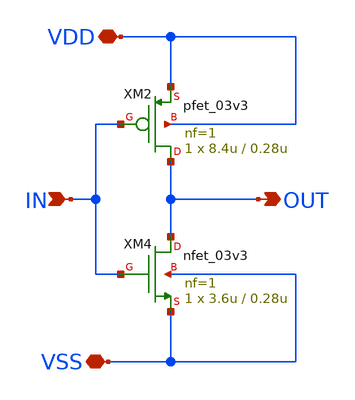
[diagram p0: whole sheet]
** sch_path: xschem/io_inv_3i.sch
* Copyright 2023 David Mitchell Bailey
* Licensed under the Apache License, Version 2.0 (the "License");
* you may not use this file except in compliance with the License.
* You may obtain a copy of the License at
* https://www.apache.org/licenses/LICENSE-2.0
* Unless required by applicable law or agreed to in writing, software
* distributed under the License is distributed on an "AS IS" BASIS,
* WITHOUT WARRANTIES OR CONDITIONS OF ANY KIND, either express or implied.
* See the License for the specific language governing permissions and
* limitations under the License.
**.subckt io_inv_3i OUT IN VDD VSS
*.opin OUT
*.ipin IN
*.iopin VDD
*.iopin VSS
XM2 OUT IN VDD VDD pfet_03v3 L=0.28u W=8.4u nf=1 ad='int((nf+1)/2) * W/nf * 0.18u' as='int((nf+2)/2) * W/nf * 0.18u'
+ pd='2*int((nf+1)/2) * (W/nf + 0.18u)' ps='2*int((nf+2)/2) * (W/nf + 0.18u)' nrd='0.18u / W' nrs='0.18u / W'
+ sa=0 sb=0 sd=0 m=1 par=1
XM4 OUT IN VSS VSS nfet_03v3 L=0.28u W=3.6u nf=1 ad='int((nf+1)/2) * W/nf * 0.18u' as='int((nf+2)/2) * W/nf * 0.18u'
+ pd='2*int((nf+1)/2) * (W/nf + 0.18u)' ps='2*int((nf+2)/2) * (W/nf + 0.18u)' nrd='0.18u / W' nrs='0.18u / W'
+ sa=0 sb=0 sd=0 m=1 par=1
**.ends
.end
